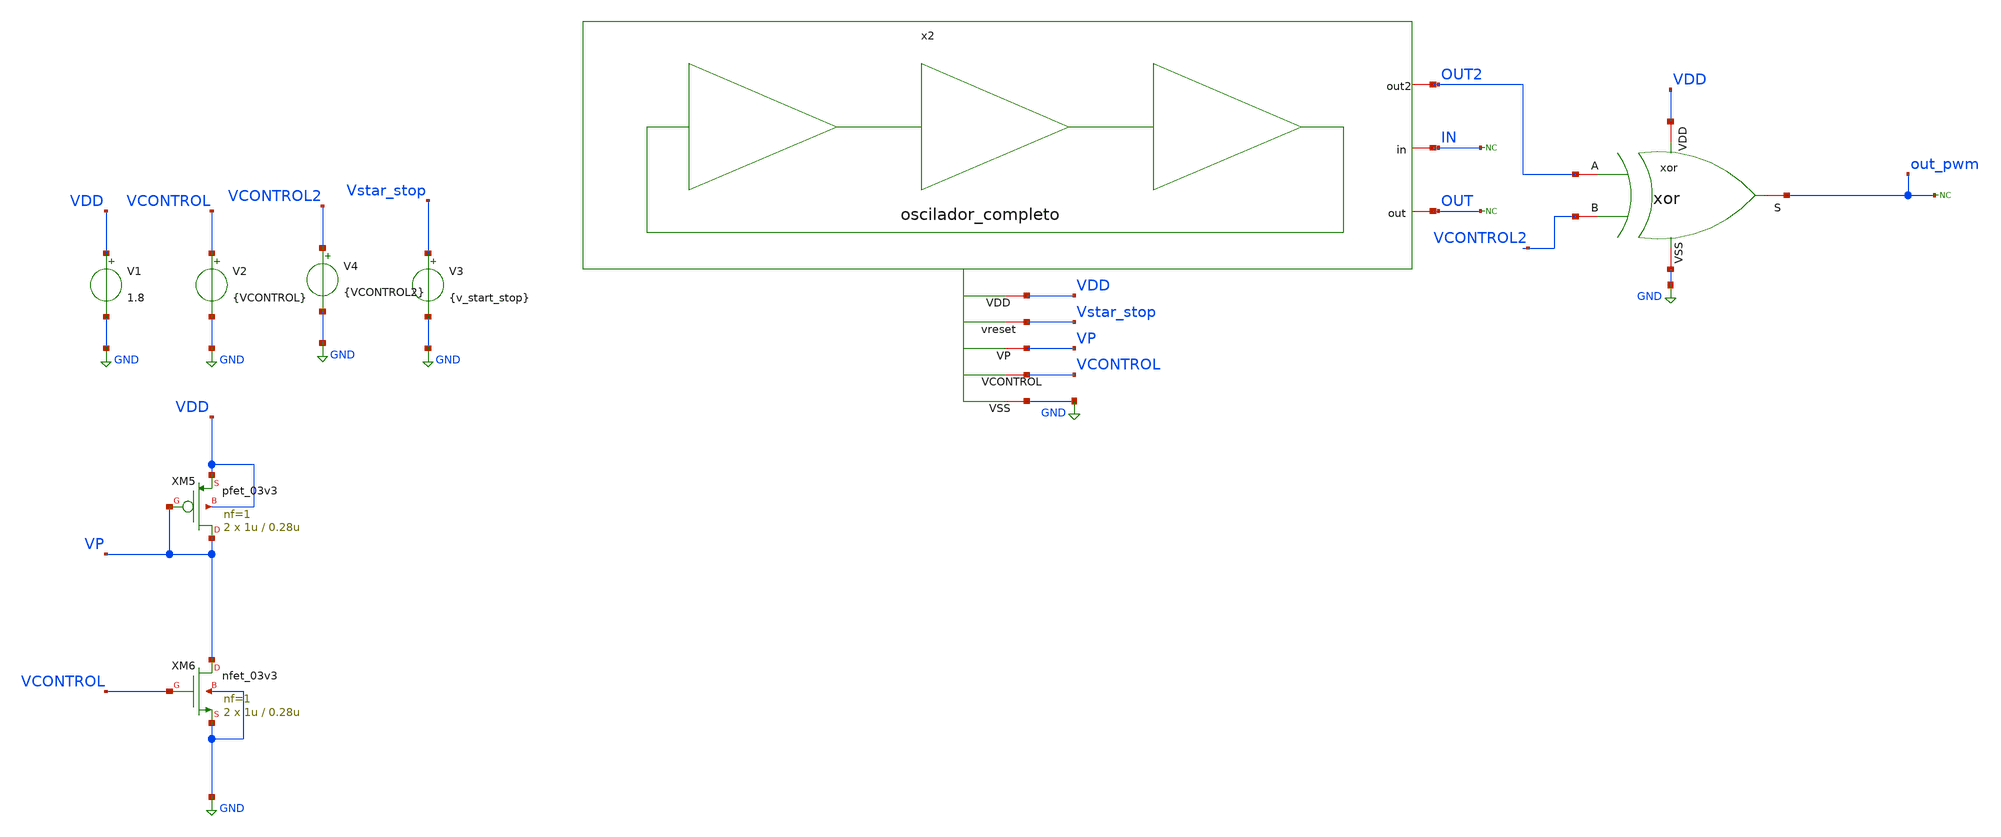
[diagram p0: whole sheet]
** sch_path: designs/ring_oscillator_pg/oscilador_con_xor.sch
**.subckt oscilador_con_xor
XM5 VP VP VDD VDD pfet_03v3 L=0.28u W=1u nf=1 ad='int((nf+1)/2) * W/nf * 0.18u' as='int((nf+2)/2) * W/nf * 0.18u'
+ pd='2*int((nf+1)/2) * (W/nf + 0.18u)' ps='2*int((nf+2)/2) * (W/nf + 0.18u)' nrd='0.18u / W' nrs='0.18u / W'
+ sa=0 sb=0 sd=0 m=2
XM6 VP VCONTROL GND GND nfet_03v3 L=0.28u W=1u nf=1 ad='int((nf+1)/2) * W/nf * 0.18u' as='int((nf+2)/2) * W/nf * 0.18u'
+ pd='2*int((nf+1)/2) * (W/nf + 0.18u)' ps='2*int((nf+2)/2) * (W/nf + 0.18u)' nrd='0.18u / W' nrs='0.18u / W'
+ sa=0 sb=0 sd=0 m=2
V1 VDD GND 1.8
V2 VCONTROL GND {VCONTROL}
V3 Vstar_stop GND {v_start_stop}
* noconn OUT
* noconn IN
* noconn out_pwm
V4 VCONTROL2 GND {VCONTROL2}
x2 OUT2 IN OUT VDD Vstar_stop VP VCONTROL GND oscilador_completo
xor VDD out_pwm OUT2 VCONTROL2 GND xor
**** begin user architecture code

.include $::180MCU_MODELS/design.ngspice
.lib $::180MCU_MODELS/sm141064.ngspice typical
.lib $::180MCU_MODELS/sm141064.ngspice res_typical





.param vcontrol=1
.param vcontrol2=1.3
.param w=1u
.param wxor=1u
.param cap=15f
.save all

.param v_start_stop=0
.control

*----------------------------- Parámetros generales
let VP = 1.8
let per50 = VP * 0.5
tran 0.01n 60n
meas TRAN T_period TRIG v(out) VAL=per50 rise=2 TARG v(out) VAL=per50 rise=3
let F_recu = 1 / T_period
meas TRAN T_period TRIG v(out) VAL=per50 rise=2 TARG v(out) VAL=per50 rise=3
print F_recu

plot v(out_pwm) v(vcontrol2) v(out2)











.endc


**** end user architecture code
**.ends

* expanding   symbol:  oscilador_completo.sym # of pins=8
** sym_path: designs/ring_oscillator_pg/oscilador_completo.sym
** sch_path: designs/ring_oscillator_pg/oscilador_completo.sch
.subckt oscilador_completo out2 in out VDD vreset VP VCONTROL VSS
*.iopin in
*.iopin out
*.iopin out2
*.iopin VDD
*.iopin VP
*.iopin VCONTROL
*.iopin VSS
*.iopin vreset
XM2 in vreset VSS VSS nfet_03v3 L=0.28u W=1u nf=1 ad='int((nf+1)/2) * W/nf * 0.18u' as='int((nf+2)/2) * W/nf * 0.18u'
+ pd='2*int((nf+1)/2) * (W/nf + 0.18u)' ps='2*int((nf+2)/2) * (W/nf + 0.18u)' nrd='0.18u / W' nrs='0.18u / W'
+ sa=0 sb=0 sd=0 m=2
x1 VDD VP in out2 VCONTROL VSS inversor
x2 VDD VP out in VCONTROL VSS inversor
x3 VDD VP out2 out VCONTROL VSS inversor
.ends


* expanding   symbol:  xor.sym # of pins=5
** sym_path: designs/ring_oscillator_pg/xor.sym
** sch_path: designs/ring_oscillator_pg/xor.sch
.subckt xor VDD S A B VSS
*.iopin VSS
*.iopin VDD
*.iopin S
*.iopin A
*.iopin B
XM2 net1 A net2 VSS nfet_03v3 L=0.28u W={wxor} nf=1 ad='int((nf+1)/2) * W/nf * 0.18u' as='int((nf+2)/2) * W/nf * 0.18u'
+ pd='2*int((nf+1)/2) * (W/nf + 0.18u)' ps='2*int((nf+2)/2) * (W/nf + 0.18u)' nrd='0.18u / W' nrs='0.18u / W'
+ sa=0 sb=0 sd=0 m=1
XM3 net1 -B net4 VDD pfet_03v3 L=0.28u W={wxor} nf=1 ad='int((nf+1)/2) * W/nf * 0.18u' as='int((nf+2)/2) * W/nf * 0.18u'
+ pd='2*int((nf+1)/2) * (W/nf + 0.18u)' ps='2*int((nf+2)/2) * (W/nf + 0.18u)' nrd='0.18u / W' nrs='0.18u / W'
+ sa=0 sb=0 sd=0 m=2
XM1 net4 A VDD VDD pfet_03v3 L=0.28u W={wxor} nf=1 ad='int((nf+1)/2) * W/nf * 0.18u' as='int((nf+2)/2) * W/nf * 0.18u'
+ pd='2*int((nf+1)/2) * (W/nf + 0.18u)' ps='2*int((nf+2)/2) * (W/nf + 0.18u)' nrd='0.18u / W' nrs='0.18u / W'
+ sa=0 sb=0 sd=0 m=2
XM4 net1 -A net3 VSS nfet_03v3 L=0.28u W={wxor} nf=1 ad='int((nf+1)/2) * W/nf * 0.18u' as='int((nf+2)/2) * W/nf * 0.18u'
+ pd='2*int((nf+1)/2) * (W/nf + 0.18u)' ps='2*int((nf+2)/2) * (W/nf + 0.18u)' nrd='0.18u / W' nrs='0.18u / W'
+ sa=0 sb=0 sd=0 m=1
XM5 net1 B net5 VDD pfet_03v3 L=0.28u W={wxor} nf=1 ad='int((nf+1)/2) * W/nf * 0.18u' as='int((nf+2)/2) * W/nf * 0.18u'
+ pd='2*int((nf+1)/2) * (W/nf + 0.18u)' ps='2*int((nf+2)/2) * (W/nf + 0.18u)' nrd='0.18u / W' nrs='0.18u / W'
+ sa=0 sb=0 sd=0 m=2
XM6 net5 -A VDD VDD pfet_03v3 L=0.28u W={wxor} nf=1 ad='int((nf+1)/2) * W/nf * 0.18u' as='int((nf+2)/2) * W/nf * 0.18u'
+ pd='2*int((nf+1)/2) * (W/nf + 0.18u)' ps='2*int((nf+2)/2) * (W/nf + 0.18u)' nrd='0.18u / W' nrs='0.18u / W'
+ sa=0 sb=0 sd=0 m=2
XM7 net2 B VSS VSS nfet_03v3 L=0.28u W={wxor} nf=1 ad='int((nf+1)/2) * W/nf * 0.18u' as='int((nf+2)/2) * W/nf * 0.18u'
+ pd='2*int((nf+1)/2) * (W/nf + 0.18u)' ps='2*int((nf+2)/2) * (W/nf + 0.18u)' nrd='0.18u / W' nrs='0.18u / W'
+ sa=0 sb=0 sd=0 m=1
XM8 net3 -B VSS VSS nfet_03v3 L=0.28u W={wxor} nf=1 ad='int((nf+1)/2) * W/nf * 0.18u' as='int((nf+2)/2) * W/nf * 0.18u'
+ pd='2*int((nf+1)/2) * (W/nf + 0.18u)' ps='2*int((nf+2)/2) * (W/nf + 0.18u)' nrd='0.18u / W' nrs='0.18u / W'
+ sa=0 sb=0 sd=0 m=1
XM9 -A A VSS VSS nfet_03v3 L=0.28u W={wxor} nf=1 ad='int((nf+1)/2) * W/nf * 0.18u' as='int((nf+2)/2) * W/nf * 0.18u'
+ pd='2*int((nf+1)/2) * (W/nf + 0.18u)' ps='2*int((nf+2)/2) * (W/nf + 0.18u)' nrd='0.18u / W' nrs='0.18u / W'
+ sa=0 sb=0 sd=0 m=1
XM10 -A A VDD VDD pfet_03v3 L=0.28u W={wxor} nf=1 ad='int((nf+1)/2) * W/nf * 0.18u' as='int((nf+2)/2) * W/nf * 0.18u'
+ pd='2*int((nf+1)/2) * (W/nf + 0.18u)' ps='2*int((nf+2)/2) * (W/nf + 0.18u)' nrd='0.18u / W' nrs='0.18u / W'
+ sa=0 sb=0 sd=0 m=2
XM11 -B B VSS VSS nfet_03v3 L=0.28u W={wxor} nf=1 ad='int((nf+1)/2) * W/nf * 0.18u' as='int((nf+2)/2) * W/nf * 0.18u'
+ pd='2*int((nf+1)/2) * (W/nf + 0.18u)' ps='2*int((nf+2)/2) * (W/nf + 0.18u)' nrd='0.18u / W' nrs='0.18u / W'
+ sa=0 sb=0 sd=0 m=1
XM12 -B B VDD VDD pfet_03v3 L=0.28u W={wxor} nf=1 ad='int((nf+1)/2) * W/nf * 0.18u' as='int((nf+2)/2) * W/nf * 0.18u'
+ pd='2*int((nf+1)/2) * (W/nf + 0.18u)' ps='2*int((nf+2)/2) * (W/nf + 0.18u)' nrd='0.18u / W' nrs='0.18u / W'
+ sa=0 sb=0 sd=0 m=2
XM13 net6 net1 VSS VSS nfet_03v3 L=0.28u W={wxor} nf=1 ad='int((nf+1)/2) * W/nf * 0.18u' as='int((nf+2)/2) * W/nf * 0.18u'
+ pd='2*int((nf+1)/2) * (W/nf + 0.18u)' ps='2*int((nf+2)/2) * (W/nf + 0.18u)' nrd='0.18u / W' nrs='0.18u / W'
+ sa=0 sb=0 sd=0 m=2
XM14 net6 net1 VDD VDD pfet_03v3 L=0.28u W={wxor} nf=1 ad='int((nf+1)/2) * W/nf * 0.18u' as='int((nf+2)/2) * W/nf * 0.18u'
+ pd='2*int((nf+1)/2) * (W/nf + 0.18u)' ps='2*int((nf+2)/2) * (W/nf + 0.18u)' nrd='0.18u / W' nrs='0.18u / W'
+ sa=0 sb=0 sd=0 m=4
XM15 S net6 VSS VSS nfet_03v3 L=0.28u W={wxor} nf=1 ad='int((nf+1)/2) * W/nf * 0.18u' as='int((nf+2)/2) * W/nf * 0.18u'
+ pd='2*int((nf+1)/2) * (W/nf + 0.18u)' ps='2*int((nf+2)/2) * (W/nf + 0.18u)' nrd='0.18u / W' nrs='0.18u / W'
+ sa=0 sb=0 sd=0 m=4
XM16 S net6 VDD VDD pfet_03v3 L=0.28u W={wxor} nf=1 ad='int((nf+1)/2) * W/nf * 0.18u' as='int((nf+2)/2) * W/nf * 0.18u'
+ pd='2*int((nf+1)/2) * (W/nf + 0.18u)' ps='2*int((nf+2)/2) * (W/nf + 0.18u)' nrd='0.18u / W' nrs='0.18u / W'
+ sa=0 sb=0 sd=0 m=8
.ends


* expanding   symbol:  gf180/ring_oscillator_pg/inversor.sym # of pins=6
** sym_path: designs/ring_oscillator_pg/inversor.sym
** sch_path: designs/ring_oscillator_pg/inversor.sch
.subckt inversor VDD VP B A VCONTROL VSS
*.iopin B
*.iopin A
*.iopin VCONTROL
*.iopin VDD
*.iopin VP
*.iopin VSS
XM1 B A net1 VSS nfet_03v3 L=0.3u W={w} nf=1 ad='int((nf+1)/2) * W/nf * 0.18u' as='int((nf+2)/2) * W/nf * 0.18u'
+ pd='2*int((nf+1)/2) * (W/nf + 0.18u)' ps='2*int((nf+2)/2) * (W/nf + 0.18u)' nrd='0.18u / W' nrs='0.18u / W'
+ sa=0 sb=0 sd=0 m=1
XM2 B A net2 VDD pfet_03v3 L=0.3u W={wp} nf=1 ad='int((nf+1)/2) * W/nf * 0.18u' as='int((nf+2)/2) * W/nf * 0.18u'
+ pd='2*int((nf+1)/2) * (W/nf + 0.18u)' ps='2*int((nf+2)/2) * (W/nf + 0.18u)' nrd='0.18u / W' nrs='0.18u / W'
+ sa=0 sb=0 sd=0 m=1
XM3 net1 VCONTROL VSS VSS nfet_03v3 L=0.3u W={w} nf=1 ad='int((nf+1)/2) * W/nf * 0.18u' as='int((nf+2)/2) * W/nf * 0.18u'
+ pd='2*int((nf+1)/2) * (W/nf + 0.18u)' ps='2*int((nf+2)/2) * (W/nf + 0.18u)' nrd='0.18u / W' nrs='0.18u / W'
+ sa=0 sb=0 sd=0 m=2
XM4 net2 VP VDD VDD pfet_03v3 L=0.3u W={wp} nf=1 ad='int((nf+1)/2) * W/nf * 0.18u' as='int((nf+2)/2) * W/nf * 0.18u'
+ pd='2*int((nf+1)/2) * (W/nf + 0.18u)' ps='2*int((nf+2)/2) * (W/nf + 0.18u)' nrd='0.18u / W' nrs='0.18u / W'
+ sa=0 sb=0 sd=0 m=1
.ends

.GLOBAL GND
.end
